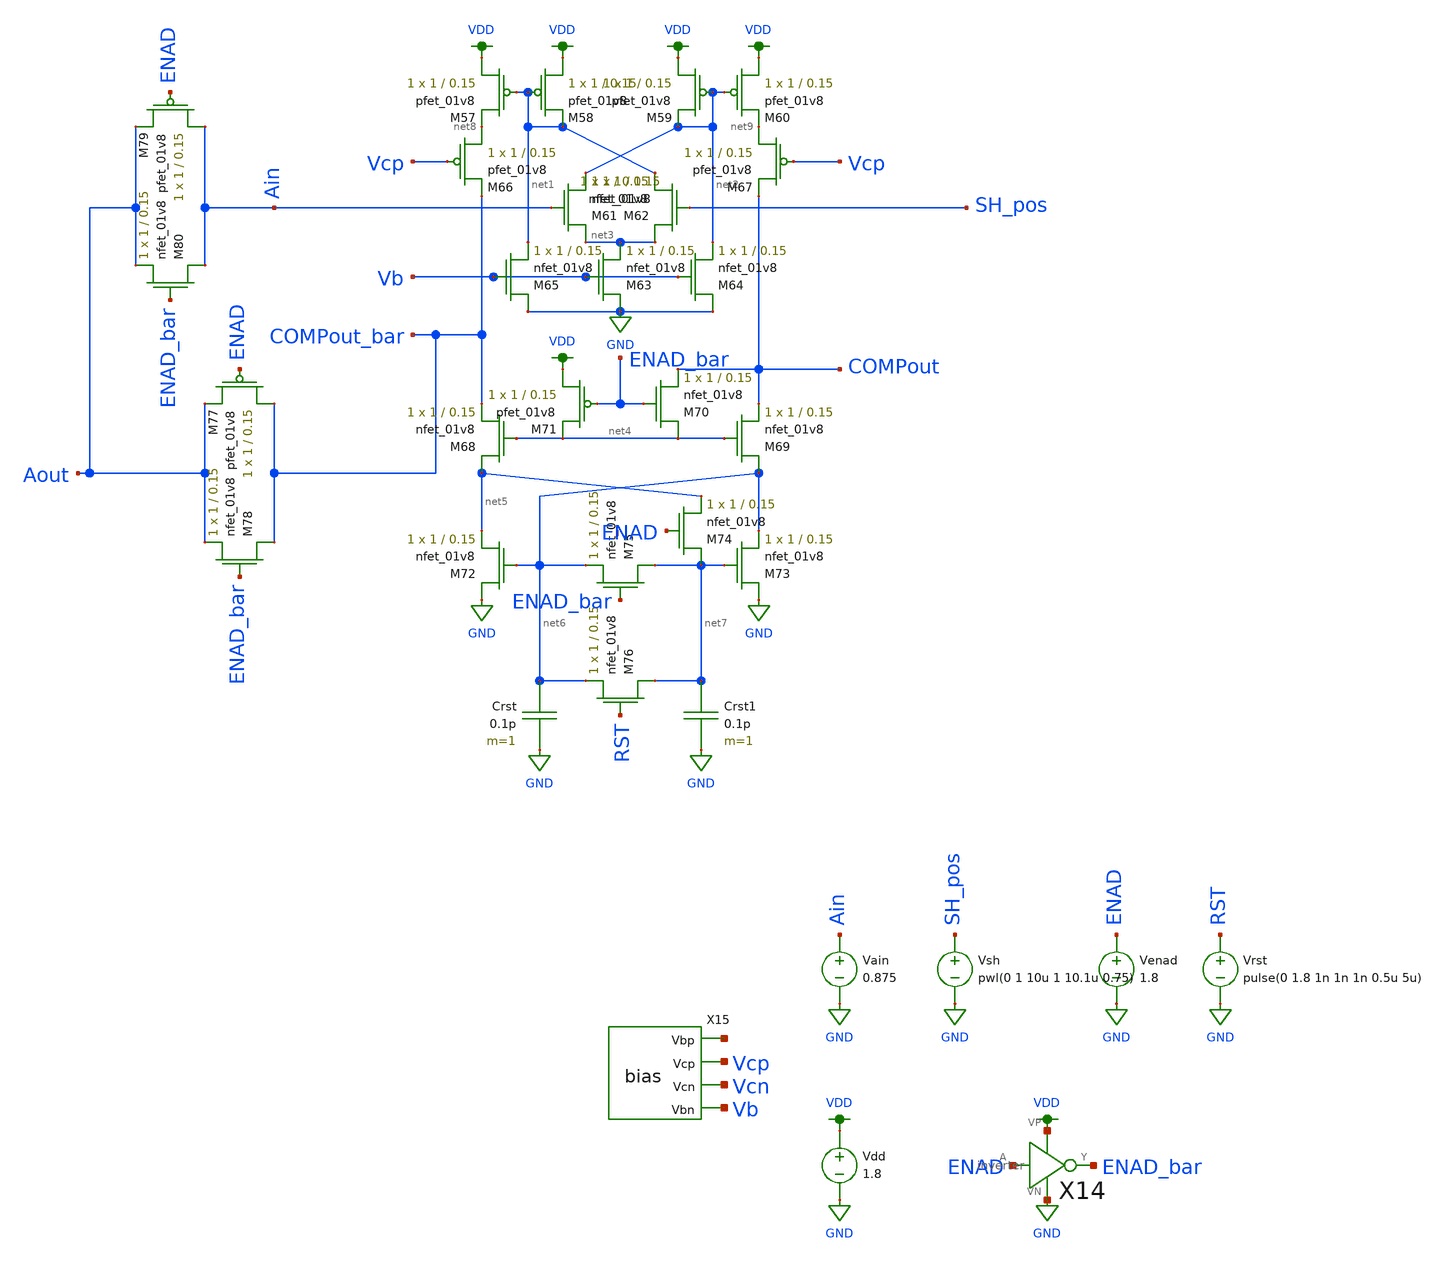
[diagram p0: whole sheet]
** sch_path: simulations/comp_test.sch
**.subckt comp_test
XM57 VDD net1 net8 VDD sky130_fd_pr__pfet_01v8 L=0.15 W=1 nf=1 ad='int((nf+1)/2) * W/nf * 0.29' as='int((nf+2)/2) * W/nf * 0.29'
+ pd='2*int((nf+1)/2) * (W/nf + 0.29)' ps='2*int((nf+2)/2) * (W/nf + 0.29)' nrd='0.29 / W' nrs='0.29 / W'
+ sa=0 sb=0 sd=0 mult=1 m=1
XM58 VDD net1 net1 VDD sky130_fd_pr__pfet_01v8 L=0.15 W=1 nf=1 ad='int((nf+1)/2) * W/nf * 0.29' as='int((nf+2)/2) * W/nf * 0.29'
+ pd='2*int((nf+1)/2) * (W/nf + 0.29)' ps='2*int((nf+2)/2) * (W/nf + 0.29)' nrd='0.29 / W' nrs='0.29 / W'
+ sa=0 sb=0 sd=0 mult=1 m=1
XM59 VDD net2 net2 VDD sky130_fd_pr__pfet_01v8 L=0.15 W=1 nf=1 ad='int((nf+1)/2) * W/nf * 0.29' as='int((nf+2)/2) * W/nf * 0.29'
+ pd='2*int((nf+1)/2) * (W/nf + 0.29)' ps='2*int((nf+2)/2) * (W/nf + 0.29)' nrd='0.29 / W' nrs='0.29 / W'
+ sa=0 sb=0 sd=0 mult=1 m=1
XM60 VDD net2 net9 VDD sky130_fd_pr__pfet_01v8 L=0.15 W=1 nf=1 ad='int((nf+1)/2) * W/nf * 0.29' as='int((nf+2)/2) * W/nf * 0.29'
+ pd='2*int((nf+1)/2) * (W/nf + 0.29)' ps='2*int((nf+2)/2) * (W/nf + 0.29)' nrd='0.29 / W' nrs='0.29 / W'
+ sa=0 sb=0 sd=0 mult=1 m=1
XM61 net3 Ain net2 GND sky130_fd_pr__nfet_01v8 L=0.15 W=1 nf=1 ad='int((nf+1)/2) * W/nf * 0.29' as='int((nf+2)/2) * W/nf * 0.29'
+ pd='2*int((nf+1)/2) * (W/nf + 0.29)' ps='2*int((nf+2)/2) * (W/nf + 0.29)' nrd='0.29 / W' nrs='0.29 / W'
+ sa=0 sb=0 sd=0 mult=1 m=1
XM62 net3 SH_pos net1 GND sky130_fd_pr__nfet_01v8 L=0.15 W=1 nf=1 ad='int((nf+1)/2) * W/nf * 0.29' as='int((nf+2)/2) * W/nf * 0.29'
+ pd='2*int((nf+1)/2) * (W/nf + 0.29)' ps='2*int((nf+2)/2) * (W/nf + 0.29)' nrd='0.29 / W' nrs='0.29 / W'
+ sa=0 sb=0 sd=0 mult=1 m=1
XM63 GND Vb net3 GND sky130_fd_pr__nfet_01v8 L=0.15 W=1 nf=1 ad='int((nf+1)/2) * W/nf * 0.29' as='int((nf+2)/2) * W/nf * 0.29'
+ pd='2*int((nf+1)/2) * (W/nf + 0.29)' ps='2*int((nf+2)/2) * (W/nf + 0.29)' nrd='0.29 / W' nrs='0.29 / W'
+ sa=0 sb=0 sd=0 mult=1 m=1
XM64 GND Vb net2 GND sky130_fd_pr__nfet_01v8 L=0.15 W=1 nf=1 ad='int((nf+1)/2) * W/nf * 0.29' as='int((nf+2)/2) * W/nf * 0.29'
+ pd='2*int((nf+1)/2) * (W/nf + 0.29)' ps='2*int((nf+2)/2) * (W/nf + 0.29)' nrd='0.29 / W' nrs='0.29 / W'
+ sa=0 sb=0 sd=0 mult=1 m=1
XM65 GND Vb net1 GND sky130_fd_pr__nfet_01v8 L=0.15 W=1 nf=1 ad='int((nf+1)/2) * W/nf * 0.29' as='int((nf+2)/2) * W/nf * 0.29'
+ pd='2*int((nf+1)/2) * (W/nf + 0.29)' ps='2*int((nf+2)/2) * (W/nf + 0.29)' nrd='0.29 / W' nrs='0.29 / W'
+ sa=0 sb=0 sd=0 mult=1 m=1
XM66 net8 Vcp COMPout_bar VDD sky130_fd_pr__pfet_01v8 L=0.15 W=1 nf=1 ad='int((nf+1)/2) * W/nf * 0.29'
+ as='int((nf+2)/2) * W/nf * 0.29' pd='2*int((nf+1)/2) * (W/nf + 0.29)' ps='2*int((nf+2)/2) * (W/nf + 0.29)'
+ nrd='0.29 / W' nrs='0.29 / W' sa=0 sb=0 sd=0 mult=1 m=1
XM67 net9 Vcp COMPout VDD sky130_fd_pr__pfet_01v8 L=0.15 W=1 nf=1 ad='int((nf+1)/2) * W/nf * 0.29' as='int((nf+2)/2) * W/nf * 0.29'
+ pd='2*int((nf+1)/2) * (W/nf + 0.29)' ps='2*int((nf+2)/2) * (W/nf + 0.29)' nrd='0.29 / W' nrs='0.29 / W'
+ sa=0 sb=0 sd=0 mult=1 m=1
XM68 net5 net4 COMPout_bar GND sky130_fd_pr__nfet_01v8 L=0.15 W=1 nf=1 ad='int((nf+1)/2) * W/nf * 0.29'
+ as='int((nf+2)/2) * W/nf * 0.29' pd='2*int((nf+1)/2) * (W/nf + 0.29)' ps='2*int((nf+2)/2) * (W/nf + 0.29)'
+ nrd='0.29 / W' nrs='0.29 / W' sa=0 sb=0 sd=0 mult=1 m=1
XM69 net6 net4 COMPout GND sky130_fd_pr__nfet_01v8 L=0.15 W=1 nf=1 ad='int((nf+1)/2) * W/nf * 0.29' as='int((nf+2)/2) * W/nf * 0.29'
+ pd='2*int((nf+1)/2) * (W/nf + 0.29)' ps='2*int((nf+2)/2) * (W/nf + 0.29)' nrd='0.29 / W' nrs='0.29 / W'
+ sa=0 sb=0 sd=0 mult=1 m=1
XM70 net4 ENAD_bar COMPout GND sky130_fd_pr__nfet_01v8 L=0.15 W=1 nf=1 ad='int((nf+1)/2) * W/nf * 0.29'
+ as='int((nf+2)/2) * W/nf * 0.29' pd='2*int((nf+1)/2) * (W/nf + 0.29)' ps='2*int((nf+2)/2) * (W/nf + 0.29)'
+ nrd='0.29 / W' nrs='0.29 / W' sa=0 sb=0 sd=0 mult=1 m=1
XM71 VDD ENAD_bar net4 VDD sky130_fd_pr__pfet_01v8 L=0.15 W=1 nf=1 ad='int((nf+1)/2) * W/nf * 0.29' as='int((nf+2)/2) * W/nf * 0.29'
+ pd='2*int((nf+1)/2) * (W/nf + 0.29)' ps='2*int((nf+2)/2) * (W/nf + 0.29)' nrd='0.29 / W' nrs='0.29 / W'
+ sa=0 sb=0 sd=0 mult=1 m=1
XM72 GND net6 net5 GND sky130_fd_pr__nfet_01v8 L=0.15 W=1 nf=1 ad='int((nf+1)/2) * W/nf * 0.29' as='int((nf+2)/2) * W/nf * 0.29'
+ pd='2*int((nf+1)/2) * (W/nf + 0.29)' ps='2*int((nf+2)/2) * (W/nf + 0.29)' nrd='0.29 / W' nrs='0.29 / W'
+ sa=0 sb=0 sd=0 mult=1 m=1
XM73 GND net7 net6 GND sky130_fd_pr__nfet_01v8 L=0.15 W=1 nf=1 ad='int((nf+1)/2) * W/nf * 0.29' as='int((nf+2)/2) * W/nf * 0.29'
+ pd='2*int((nf+1)/2) * (W/nf + 0.29)' ps='2*int((nf+2)/2) * (W/nf + 0.29)' nrd='0.29 / W' nrs='0.29 / W'
+ sa=0 sb=0 sd=0 mult=1 m=1
XM74 net7 ENAD net5 GND sky130_fd_pr__nfet_01v8 L=0.15 W=1 nf=1 ad='int((nf+1)/2) * W/nf * 0.29' as='int((nf+2)/2) * W/nf * 0.29'
+ pd='2*int((nf+1)/2) * (W/nf + 0.29)' ps='2*int((nf+2)/2) * (W/nf + 0.29)' nrd='0.29 / W' nrs='0.29 / W'
+ sa=0 sb=0 sd=0 mult=1 m=1
XM75 net7 ENAD_bar net6 GND sky130_fd_pr__nfet_01v8 L=0.15 W=1 nf=1 ad='int((nf+1)/2) * W/nf * 0.29'
+ as='int((nf+2)/2) * W/nf * 0.29' pd='2*int((nf+1)/2) * (W/nf + 0.29)' ps='2*int((nf+2)/2) * (W/nf + 0.29)'
+ nrd='0.29 / W' nrs='0.29 / W' sa=0 sb=0 sd=0 mult=1 m=1
Crst net6 GND 0.1p m=1
XM76 net7 RST net6 GND sky130_fd_pr__nfet_01v8 L=0.15 W=1 nf=1 ad='int((nf+1)/2) * W/nf * 0.29' as='int((nf+2)/2) * W/nf * 0.29'
+ pd='2*int((nf+1)/2) * (W/nf + 0.29)' ps='2*int((nf+2)/2) * (W/nf + 0.29)' nrd='0.29 / W' nrs='0.29 / W'
+ sa=0 sb=0 sd=0 mult=1 m=1
Crst1 net7 GND 0.1p m=1
XM77 COMPout_bar ENAD Aout VDD sky130_fd_pr__pfet_01v8 L=0.15 W=1 nf=1 ad='int((nf+1)/2) * W/nf * 0.29'
+ as='int((nf+2)/2) * W/nf * 0.29' pd='2*int((nf+1)/2) * (W/nf + 0.29)' ps='2*int((nf+2)/2) * (W/nf + 0.29)'
+ nrd='0.29 / W' nrs='0.29 / W' sa=0 sb=0 sd=0 mult=1 m=1
XM78 COMPout_bar ENAD_bar Aout GND sky130_fd_pr__nfet_01v8 L=0.15 W=1 nf=1 ad='int((nf+1)/2) * W/nf * 0.29'
+ as='int((nf+2)/2) * W/nf * 0.29' pd='2*int((nf+1)/2) * (W/nf + 0.29)' ps='2*int((nf+2)/2) * (W/nf + 0.29)'
+ nrd='0.29 / W' nrs='0.29 / W' sa=0 sb=0 sd=0 mult=1 m=1
XM79 Ain ENAD Aout VDD sky130_fd_pr__pfet_01v8 L=0.15 W=1 nf=1 ad='int((nf+1)/2) * W/nf * 0.29' as='int((nf+2)/2) * W/nf * 0.29'
+ pd='2*int((nf+1)/2) * (W/nf + 0.29)' ps='2*int((nf+2)/2) * (W/nf + 0.29)' nrd='0.29 / W' nrs='0.29 / W'
+ sa=0 sb=0 sd=0 mult=1 m=1
XM80 Ain ENAD_bar Aout GND sky130_fd_pr__nfet_01v8 L=0.15 W=1 nf=1 ad='int((nf+1)/2) * W/nf * 0.29' as='int((nf+2)/2) * W/nf * 0.29'
+ pd='2*int((nf+1)/2) * (W/nf + 0.29)' ps='2*int((nf+2)/2) * (W/nf + 0.29)' nrd='0.29 / W' nrs='0.29 / W'
+ sa=0 sb=0 sd=0 mult=1 m=1
Venad ENAD GND 1.8
X14 ENAD ENAD_bar VDD GND inverter
Vdd VDD GND 1.8
Vain Ain GND 0.875
X15 net10 Vcp Vcn Vb bias
Vsh SH_pos GND pwl(0 1 10u 1 10.1u 0.75)
Vrst RST GND pulse(0 1.8 1n 1n 1n 0.5u 5u)
**** begin user architecture code

.option wnflag=1
.param MC_SWITCH=0.0
.lib ~/skywater/skywater-pdk/libraries/sky130_fd_pr_ngspice/latest/models/sky130.lib.spice tt


.tran 1n 20u
.save all

**** end user architecture code
**.ends

* expanding   symbol:  ../schematics/inverter.sym # of pins=4
** sym_path: schematics/inverter.sym
** sch_path: schematics/inverter.sch
.subckt inverter A Y VP VN
*.ipin A
*.iopin VP
*.iopin VN
*.opin Y
XM1 Y A VP VDD sky130_fd_pr__pfet_01v8 L=0.15 W=1 nf=1 ad='int((nf+1)/2) * W/nf * 0.29' as='int((nf+2)/2) * W/nf * 0.29'
+ pd='2*int((nf+1)/2) * (W/nf + 0.29)' ps='2*int((nf+2)/2) * (W/nf + 0.29)' nrd='0.29 / W' nrs='0.29 / W'
+ sa=0 sb=0 sd=0 mult=1 m=1
XM2 Y A VN GND sky130_fd_pr__nfet_01v8 L=0.15 W=1 nf=1 ad='int((nf+1)/2) * W/nf * 0.29' as='int((nf+2)/2) * W/nf * 0.29'
+ pd='2*int((nf+1)/2) * (W/nf + 0.29)' ps='2*int((nf+2)/2) * (W/nf + 0.29)' nrd='0.29 / W' nrs='0.29 / W'
+ sa=0 sb=0 sd=0 mult=1 m=1
.ends


* expanding   symbol:  ../schematics/bias.sym # of pins=4
** sym_path: schematics/bias.sym
** sch_path: schematics/bias.sch
.subckt bias Vbp Vcp Vcn Vbn
*.opin Vcp
*.opin Vcn
*.opin Vbn
*.opin Vbp
XM1 net1 Vbn GND GND sky130_fd_pr__nfet_01v8 L=2.5 W=12 nf=1 ad='int((nf+1)/2) * W/nf * 0.29' as='int((nf+2)/2) * W/nf * 0.29'
+ pd='2*int((nf+1)/2) * (W/nf + 0.29)' ps='2*int((nf+2)/2) * (W/nf + 0.29)' nrd='0.29 / W' nrs='0.29 / W'
+ sa=0 sb=0 sd=0 mult=1 m=1
XM2 Vcp Vbn GND GND sky130_fd_pr__nfet_01v8 L=0.5 W=12 nf=1 ad='int((nf+1)/2) * W/nf * 0.29' as='int((nf+2)/2) * W/nf * 0.29'
+ pd='2*int((nf+1)/2) * (W/nf + 0.29)' ps='2*int((nf+2)/2) * (W/nf + 0.29)' nrd='0.29 / W' nrs='0.29 / W'
+ sa=0 sb=0 sd=0 mult=1 m=1
XM3 Vbp Vbn GND GND sky130_fd_pr__nfet_01v8 L=0.5 W=12 nf=1 ad='int((nf+1)/2) * W/nf * 0.29' as='int((nf+2)/2) * W/nf * 0.29'
+ pd='2*int((nf+1)/2) * (W/nf + 0.29)' ps='2*int((nf+2)/2) * (W/nf + 0.29)' nrd='0.29 / W' nrs='0.29 / W'
+ sa=0 sb=0 sd=0 mult=1 m=1
XM4 net3 net4 GND GND sky130_fd_pr__nfet_01v8 L=0.5 W=12 nf=1 ad='int((nf+1)/2) * W/nf * 0.29' as='int((nf+2)/2) * W/nf * 0.29'
+ pd='2*int((nf+1)/2) * (W/nf + 0.29)' ps='2*int((nf+2)/2) * (W/nf + 0.29)' nrd='0.29 / W' nrs='0.29 / W'
+ sa=0 sb=0 sd=0 mult=1 m=1
XM5 Vbn Vbn GND GND sky130_fd_pr__nfet_01v8 L=0.5 W=12 nf=1 ad='int((nf+1)/2) * W/nf * 0.29' as='int((nf+2)/2) * W/nf * 0.29'
+ pd='2*int((nf+1)/2) * (W/nf + 0.29)' ps='2*int((nf+2)/2) * (W/nf + 0.29)' nrd='0.29 / W' nrs='0.29 / W'
+ sa=0 sb=0 sd=0 mult=1 m=1
XM6 net4 net4 net3 GND sky130_fd_pr__nfet_01v8 L=0.5 W=48 nf=1 ad='int((nf+1)/2) * W/nf * 0.29' as='int((nf+2)/2) * W/nf * 0.29'
+ pd='2*int((nf+1)/2) * (W/nf + 0.29)' ps='2*int((nf+2)/2) * (W/nf + 0.29)' nrd='0.29 / W' nrs='0.29 / W'
+ sa=0 sb=0 sd=0 mult=1 m=1
XM7 Vcn Vcn net3 GND sky130_fd_pr__nfet_01v8 L=0.5 W=12 nf=1 ad='int((nf+1)/2) * W/nf * 0.29' as='int((nf+2)/2) * W/nf * 0.29'
+ pd='2*int((nf+1)/2) * (W/nf + 0.29)' ps='2*int((nf+2)/2) * (W/nf + 0.29)' nrd='0.29 / W' nrs='0.29 / W'
+ sa=0 sb=0 sd=0 mult=1 m=1
XM8 net1 net1 net2 VDD sky130_fd_pr__pfet_01v8 L=0.5 W=48 nf=1 ad='int((nf+1)/2) * W/nf * 0.29' as='int((nf+2)/2) * W/nf * 0.29'
+ pd='2*int((nf+1)/2) * (W/nf + 0.29)' ps='2*int((nf+2)/2) * (W/nf + 0.29)' nrd='0.29 / W' nrs='0.29 / W'
+ sa=0 sb=0 sd=0 mult=1 m=1
XM9 net2 net1 VDD VDD sky130_fd_pr__pfet_01v8 L=0.5 W=12 nf=1 ad='int((nf+1)/2) * W/nf * 0.29' as='int((nf+2)/2) * W/nf * 0.29'
+ pd='2*int((nf+1)/2) * (W/nf + 0.29)' ps='2*int((nf+2)/2) * (W/nf + 0.29)' nrd='0.29 / W' nrs='0.29 / W'
+ sa=0 sb=0 sd=0 mult=1 m=1
XM10 Vcp Vcp net2 VDD sky130_fd_pr__pfet_01v8 L=0.5 W=12 nf=1 ad='int((nf+1)/2) * W/nf * 0.29' as='int((nf+2)/2) * W/nf * 0.29'
+ pd='2*int((nf+1)/2) * (W/nf + 0.29)' ps='2*int((nf+2)/2) * (W/nf + 0.29)' nrd='0.29 / W' nrs='0.29 / W'
+ sa=0 sb=0 sd=0 mult=1 m=1
XM11 Vbp Vbp VDD VDD sky130_fd_pr__pfet_01v8 L=0.5 W=12 nf=1 ad='int((nf+1)/2) * W/nf * 0.29' as='int((nf+2)/2) * W/nf * 0.29'
+ pd='2*int((nf+1)/2) * (W/nf + 0.29)' ps='2*int((nf+2)/2) * (W/nf + 0.29)' nrd='0.29 / W' nrs='0.29 / W'
+ sa=0 sb=0 sd=0 mult=1 m=1
XM12 net4 Vbp VDD VDD sky130_fd_pr__pfet_01v8 L=2.5 W=12 nf=1 ad='int((nf+1)/2) * W/nf * 0.29' as='int((nf+2)/2) * W/nf * 0.29'
+ pd='2*int((nf+1)/2) * (W/nf + 0.29)' ps='2*int((nf+2)/2) * (W/nf + 0.29)' nrd='0.29 / W' nrs='0.29 / W'
+ sa=0 sb=0 sd=0 mult=1 m=1
XM13 Vcn Vbp VDD VDD sky130_fd_pr__pfet_01v8 L=0.5 W=12 nf=1 ad='int((nf+1)/2) * W/nf * 0.29' as='int((nf+2)/2) * W/nf * 0.29'
+ pd='2*int((nf+1)/2) * (W/nf + 0.29)' ps='2*int((nf+2)/2) * (W/nf + 0.29)' nrd='0.29 / W' nrs='0.29 / W'
+ sa=0 sb=0 sd=0 mult=1 m=1
I1 VDD Vbn 100u
.ends

.GLOBAL VDD
.GLOBAL GND
.end
